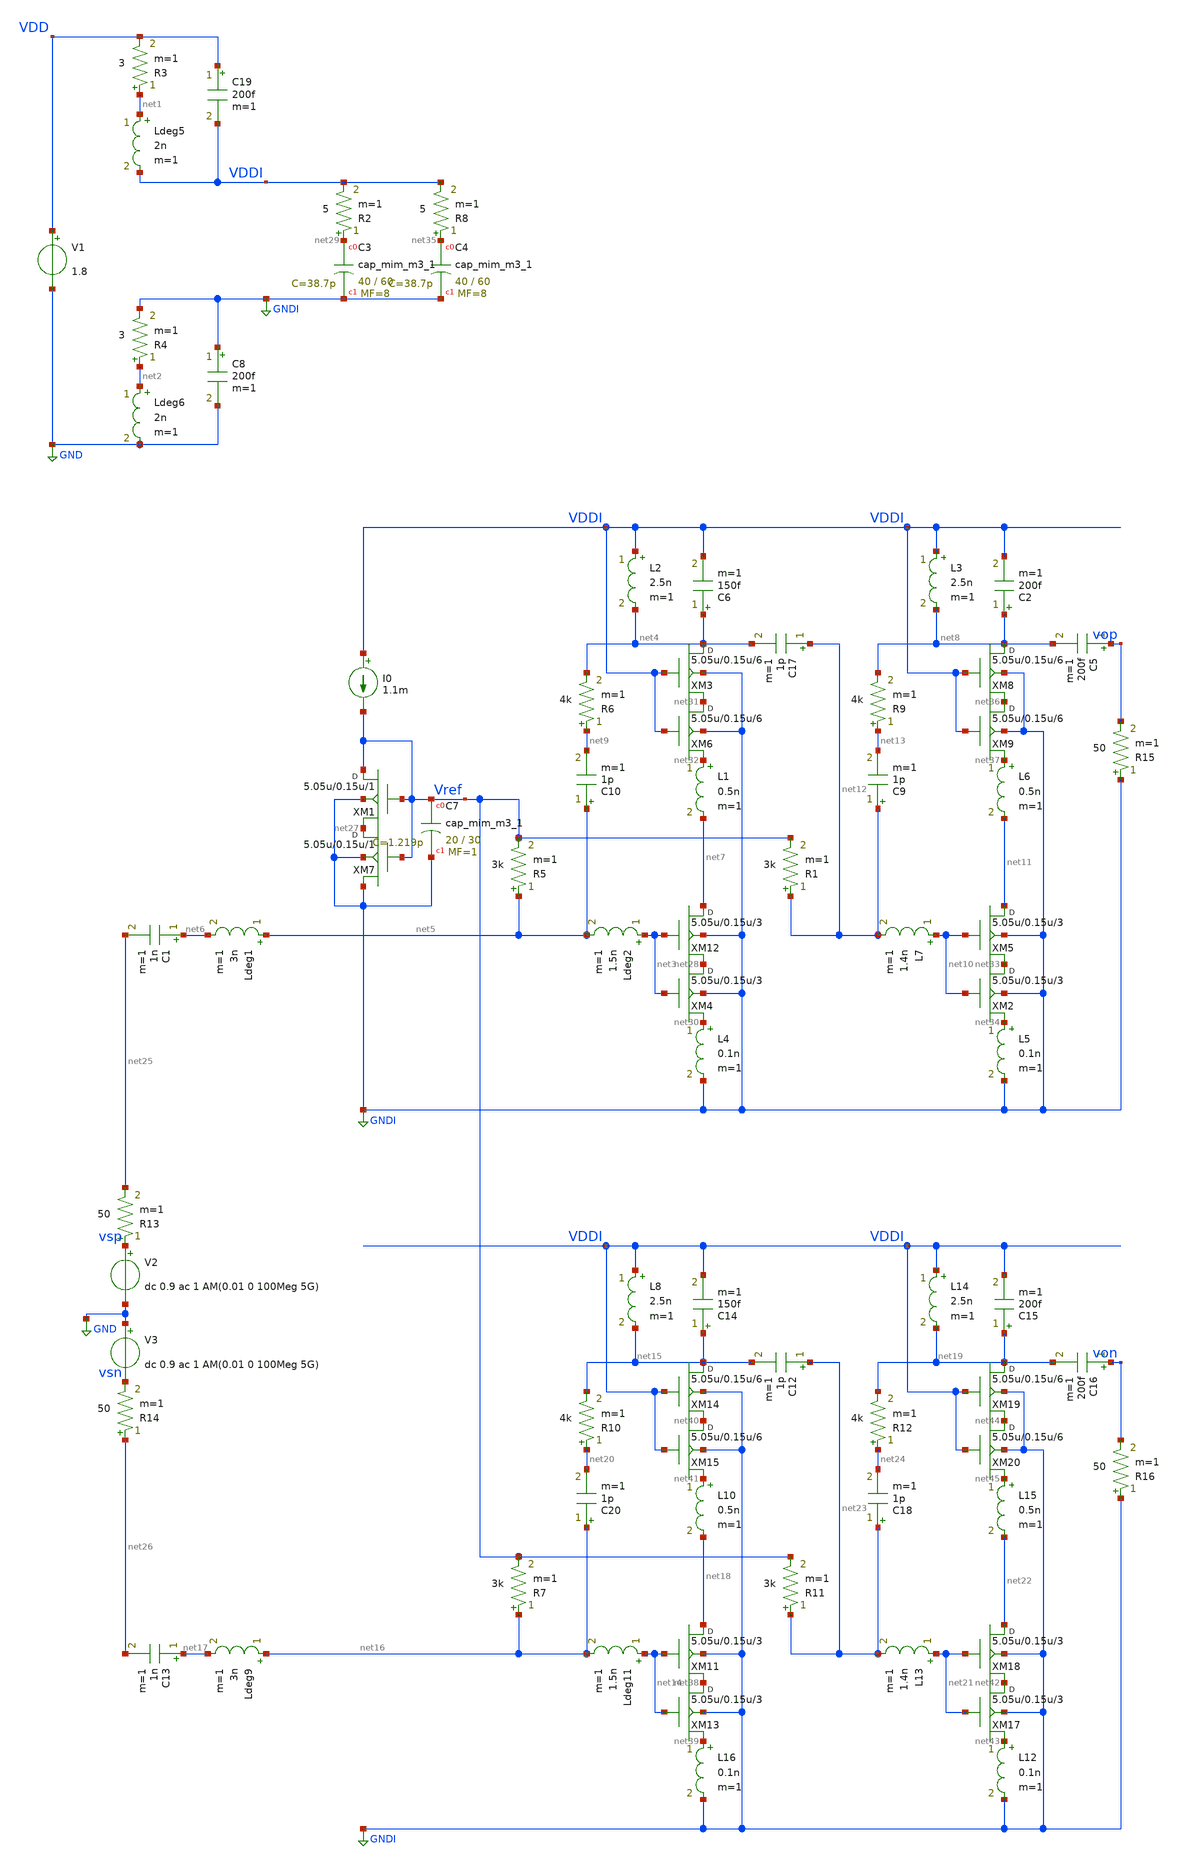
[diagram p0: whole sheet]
** sch_path: xschem/LNA5_with_output_buf_2_tran.sch
**.subckt LNA5_with_output_buf_2_tran
V1 VDD GND 1.8
V2 vsp GND dc 0.9 ac 1 AM(0.01 0 100Meg 5G)
I0 VDDI Vref 1.1m
XM1 Vref Vref net27 GNDI sky130_fd_pr__rf_nfet_01v8_bM04W5p00L0p15_ext w=5.05u l=0.15u m=1
XC7 Vref GNDI sky130_fd_pr__cap_mim_m3_1 W=20 L=30 MF=1 m=1
Ldeg5 net1 VDDI 2n m=1
R3 net1 VDD 3 m=1
Ldeg6 net2 GND 2n m=1
R4 net2 GNDI 3 m=1
XM12 net7 net3 net28 GNDI sky130_fd_pr__rf_nfet_01v8_bM04W5p00L0p15_ext w=5.05u l=0.15u m=3
C17 net12 net4 1p m=1
L2 VDDI net4 2.5n m=1
XC3 net29 GNDI sky130_fd_pr__cap_mim_m3_1 W=40 L=60 MF=8 m=8
C8 GNDI GND 200f m=1
C19 VDD VDDI 200f m=1
R2 net29 VDDI 5 m=1
R5 net5 Vref 3k m=1
XM4 net28 net3 net30 GNDI sky130_fd_pr__rf_nfet_01v8_bM04W5p00L0p15_ext w=5.05u l=0.15u m=3
C1 net6 net25 1n m=1
C6 net4 VDDI 150f m=1
R6 net9 net4 4k m=1
XM3 net4 VDDI net31 GNDI sky130_fd_pr__rf_nfet_01v8_bM04W5p00L0p15_ext w=5.05u l=0.15u m=6
XM6 net31 VDDI net32 GNDI sky130_fd_pr__rf_nfet_01v8_bM04W5p00L0p15_ext w=5.05u l=0.15u m=6
XM7 net27 Vref GNDI GNDI sky130_fd_pr__rf_nfet_01v8_bM04W5p00L0p15_ext w=5.05u l=0.15u m=1
Ldeg1 net5 net6 3n m=1
L1 net32 net7 0.5n m=1
Ldeg2 net3 net5 1.5n m=1
XM2 net33 net10 net34 GNDI sky130_fd_pr__rf_nfet_01v8_bM04W5p00L0p15_ext w=5.05u l=0.15u m=3
L5 net34 GNDI 0.1n m=1
L7 net10 net12 1.4n m=1
R1 net12 Vref 3k m=1
XM5 net11 net10 net33 GNDI sky130_fd_pr__rf_nfet_01v8_bM04W5p00L0p15_ext w=5.05u l=0.15u m=3
XC4 net35 GNDI sky130_fd_pr__cap_mim_m3_1 W=40 L=60 MF=8 m=8
R8 net35 VDDI 5 m=1
L3 VDDI net8 2.5n m=1
C2 net8 VDDI 200f m=1
R9 net13 net8 4k m=1
XM8 net8 VDDI net36 GNDI sky130_fd_pr__rf_nfet_01v8_bM04W5p00L0p15_ext w=5.05u l=0.15u m=6
XM9 net36 VDDI net37 GNDI sky130_fd_pr__rf_nfet_01v8_bM04W5p00L0p15_ext w=5.05u l=0.15u m=6
L6 net37 net11 0.5n m=1
C5 vop net8 200f m=1
C9 net12 net13 1p m=1
C10 net5 net9 1p m=1
L4 net30 GNDI 0.1n m=1
XM11 net18 net14 net38 GNDI sky130_fd_pr__rf_nfet_01v8_bM04W5p00L0p15_ext w=5.05u l=0.15u m=3
C12 net23 net15 1p m=1
L8 VDDI net15 2.5n m=1
R7 net16 Vref 3k m=1
XM13 net38 net14 net39 GNDI sky130_fd_pr__rf_nfet_01v8_bM04W5p00L0p15_ext w=5.05u l=0.15u m=3
C13 net17 net26 1n m=1
C14 net15 VDDI 150f m=1
R10 net20 net15 4k m=1
XM14 net15 VDDI net40 GNDI sky130_fd_pr__rf_nfet_01v8_bM04W5p00L0p15_ext w=5.05u l=0.15u m=6
XM15 net40 VDDI net41 GNDI sky130_fd_pr__rf_nfet_01v8_bM04W5p00L0p15_ext w=5.05u l=0.15u m=6
Ldeg9 net16 net17 3n m=1
L10 net41 net18 0.5n m=1
Ldeg11 net14 net16 1.5n m=1
XM17 net42 net21 net43 GNDI sky130_fd_pr__rf_nfet_01v8_bM04W5p00L0p15_ext w=5.05u l=0.15u m=3
L12 net43 GNDI 0.1n m=1
L13 net21 net23 1.4n m=1
R11 net23 Vref 3k m=1
XM18 net22 net21 net42 GNDI sky130_fd_pr__rf_nfet_01v8_bM04W5p00L0p15_ext w=5.05u l=0.15u m=3
L14 VDDI net19 2.5n m=1
C15 net19 VDDI 200f m=1
R12 net24 net19 4k m=1
XM19 net19 VDDI net44 GNDI sky130_fd_pr__rf_nfet_01v8_bM04W5p00L0p15_ext w=5.05u l=0.15u m=6
XM20 net44 VDDI net45 GNDI sky130_fd_pr__rf_nfet_01v8_bM04W5p00L0p15_ext w=5.05u l=0.15u m=6
L15 net45 net22 0.5n m=1
C16 von net19 200f m=1
C18 net23 net24 1p m=1
C20 net16 net20 1p m=1
L16 net39 GNDI 0.1n m=1
R13 vsp net25 50 m=1
R14 net26 vsn 50 m=1
R15 GNDI vop 50 m=1
R16 GNDI von 50 m=1
V3 GND vsn dc 0.9 ac 1 AM(0.01 0 100Meg 5G)
**** begin user architecture code
.lib $::SKYWATER_MODELS/sky130.lib.spice tt
* .include $::PDKPATH/libs.ref/sky130_fd_sc_hvl/spice/sky130_fd_sc_hvl.spice



.subckt sky130_fd_pr__rf_nfet_01v8_bM04W5p00L0p15_ext DRAIN GATE SOURCE SUBSTRATE
X0 DRAIN GATE SOURCE SUBSTRATE sky130_fd_pr__nfet_01v8 ad=2.828e+12p pd=2.132e+07u as=4.242e+12p
+ ps=3.198e+07u w=5.05e+06u l=150000u
X1 SOURCE SUBSTRATE SUBSTRATE SUBSTRATE sky130_fd_pr__nfet_01v8 ad=0p pd=0u as=3.03e+12p
+ ps=2.14e+07u w=5.05e+06u l=150000u
X2 SOURCE GATE DRAIN SUBSTRATE sky130_fd_pr__nfet_01v8 ad=0p pd=0u as=0p ps=0u w=5.05e+06u l=150000u
X3 DRAIN GATE SOURCE SUBSTRATE sky130_fd_pr__nfet_01v8 ad=0p pd=0u as=0p ps=0u w=5.05e+06u l=150000u
X4 SUBSTRATE SUBSTRATE SOURCE SUBSTRATE sky130_fd_pr__nfet_01v8 ad=0p pd=0u as=0p ps=0u w=5.05e+06u
+ l=150000u
X5 SOURCE GATE DRAIN SUBSTRATE sky130_fd_pr__nfet_01v8 ad=0p pd=0u as=0p ps=0u w=5.05e+06u l=150000u
.ends
.tran 5ps 100ns
* .ac dec 1000 0.01e9 100e9
.control
run
display
let vo=vop-von
let vs=vsp-vsn
.endc


**** end user architecture code
**.ends
.GLOBAL GND
.GLOBAL GNDI
.end
